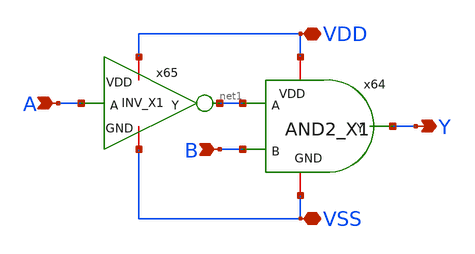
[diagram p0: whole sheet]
** sch_path: Vol.2/files/04/xschem/AND_Ainv.sch
**.subckt AND_Ainv VDD VSS Y A B
*.iopin VDD
*.iopin VSS
*.opin Y
*.ipin A
*.ipin B
x64 VDD Y net1 B VSS AND2_X1
x65 VDD A net1 VSS INV_X1
**.ends

* expanding   symbol:  IP62_5_stdcell/AND2_X1.sym # of pins=5
** sym_path: IP62_5_stdcell/AND2_X1.sym
** sch_path: IP62_5_stdcell/AND2_X1.sch
.subckt AND2_X1 VDD Y A B GND
*.opin Y
*.ipin A
*.ipin B
*.iopin VDD
*.iopin GND
XM7 net1 B VDD VDD PMOS w=10.2u l=1u as=0 ad=0 ps=0 pd=0 nrd=0 nrs=0 m=1
XM1 net1 A VDD VDD PMOS w=10.2u l=1u as=0 ad=0 ps=0 pd=0 nrd=0 nrs=0 m=1
XM2 Y net1 VDD VDD PMOS w=10.2u l=1u as=0 ad=0 ps=0 pd=0 nrd=0 nrs=0 m=1
XM3 Y net1 GND GND NMOS w=3.4u l=1u as=0 ad=0 ps=0 pd=0 nrd=0 nrs=0 m=1
XM4 net1 A net2 GND NMOS w=3.4u l=1u as=0 ad=0 ps=0 pd=0 nrd=0 nrs=0 m=1
XM5 net2 B GND GND NMOS w=3.4u l=1u as=0 ad=0 ps=0 pd=0 nrd=0 nrs=0 m=1
.ends


* expanding   symbol:  IP62_5_stdcell/INV_X1.sym # of pins=4
** sym_path: IP62_5_stdcell/INV_X1.sym
** sch_path: IP62_5_stdcell/INV_X1.sch
.subckt INV_X1 VDD A Y GND
*.ipin A
*.opin Y
*.iopin GND
*.iopin VDD
XM7 Y A VDD VDD PMOS w=10.2u l=1u as=0 ad=0 ps=0 pd=0 nrd=0 nrs=0 m=1
XM2 Y A GND GND NMOS w=3.4u l=1u as=0 ad=0 ps=0 pd=0 nrd=0 nrs=0 m=1
.ends

.end
